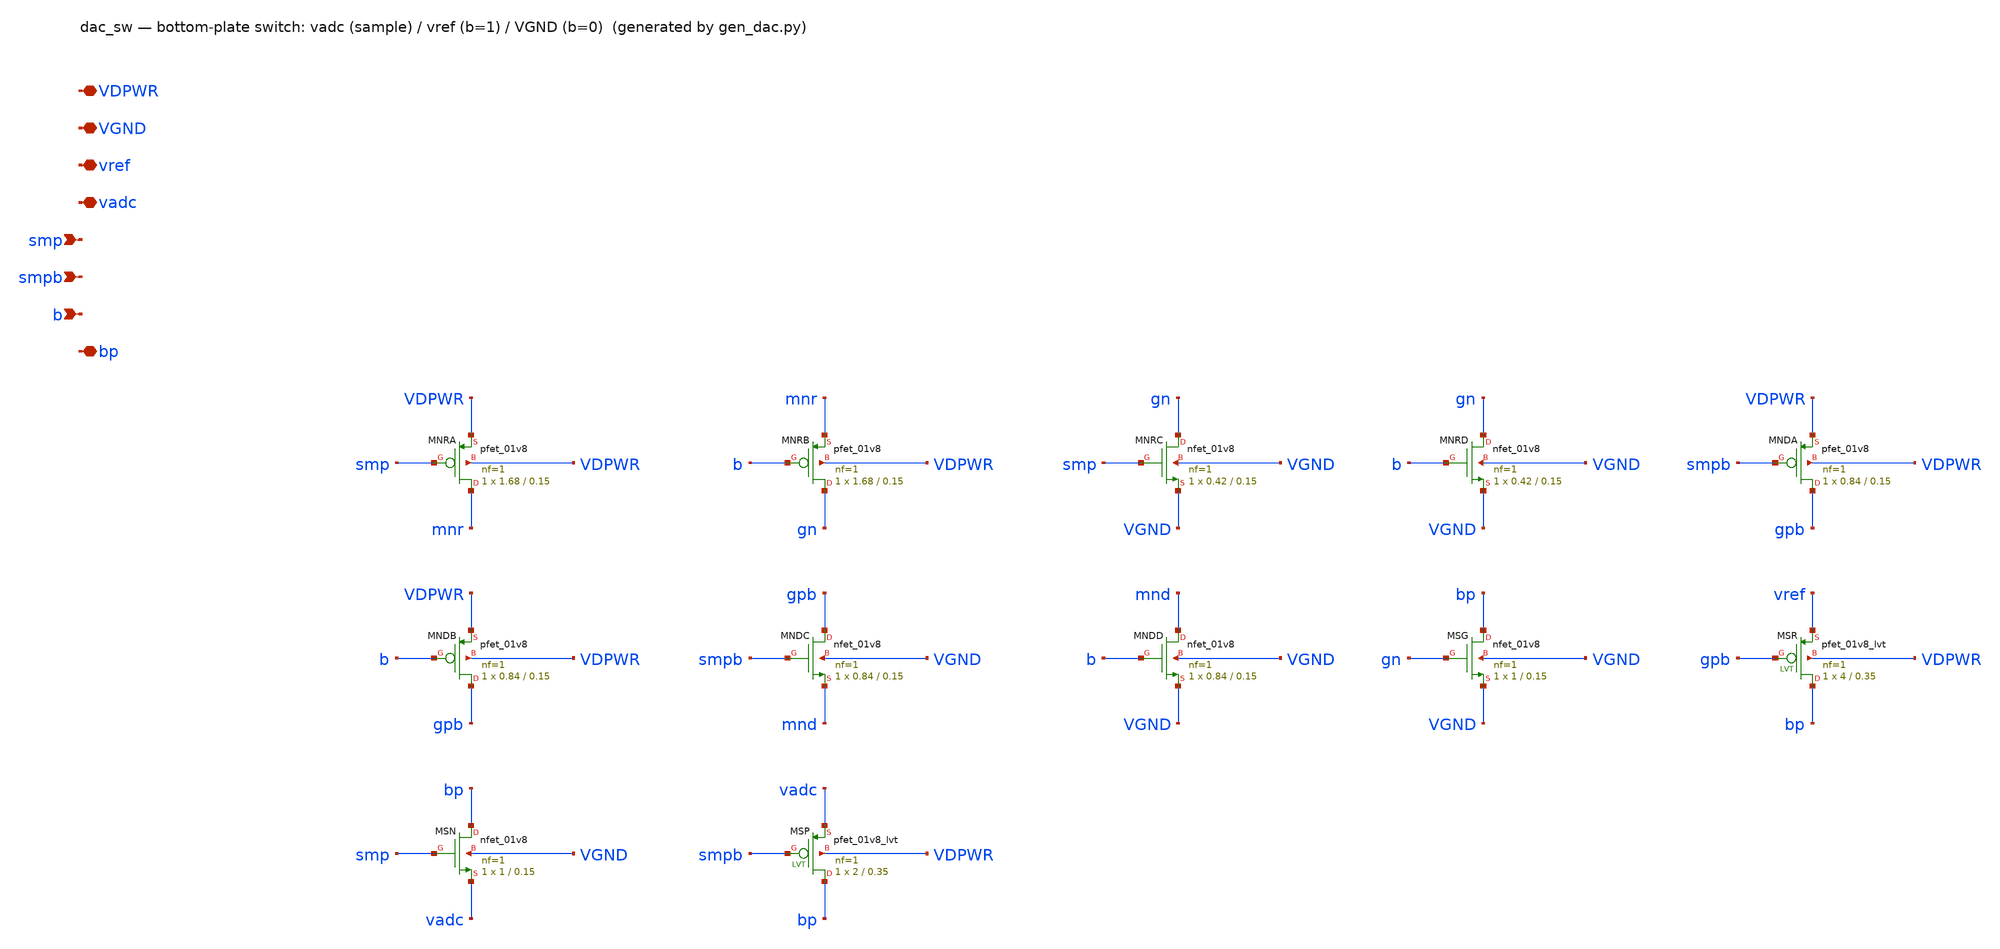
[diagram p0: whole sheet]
** sch_path: xschem/dac_sw.sch
**.subckt dac_sw VDPWR VGND vref vadc smp smpb b bp
*.iopin VDPWR
*.iopin VGND
*.iopin vref
*.iopin vadc
*.ipin smp
*.ipin smpb
*.ipin b
*.iopin bp
XMNRA mnr smp VDPWR VDPWR sky130_fd_pr__pfet_01v8 L=0.15 W=1.68 nf=1 ad='int((nf+1)/2) * W/nf * 0.29'
+ as='int((nf+2)/2) * W/nf * 0.29' pd='2*int((nf+1)/2) * (W/nf + 0.29)' ps='2*int((nf+2)/2) * (W/nf + 0.29)'
+ nrd='0.29 / W' nrs='0.29 / W' sa=0 sb=0 sd=0 mult=1 m=1
XMNRB gn b mnr VDPWR sky130_fd_pr__pfet_01v8 L=0.15 W=1.68 nf=1 ad='int((nf+1)/2) * W/nf * 0.29' as='int((nf+2)/2) * W/nf * 0.29'
+ pd='2*int((nf+1)/2) * (W/nf + 0.29)' ps='2*int((nf+2)/2) * (W/nf + 0.29)' nrd='0.29 / W' nrs='0.29 / W'
+ sa=0 sb=0 sd=0 mult=1 m=1
XMNRC gn smp VGND VGND sky130_fd_pr__nfet_01v8 L=0.15 W=0.42 nf=1 ad='int((1 + 1)/2) * 0.42 / 1 * 0.29'
+ as='int((1 + 2)/2) * 0.42 / 1 * 0.29' pd='2*int((1 + 1)/2) * (0.42 / 1 + 0.29)' ps='2*int((1 + 2)/2) * (0.42 / 1 + 0.29)'
+ nrd='0.29 / 0.42 ' nrs='0.29 / 0.42 ' sa=0 sb=0 sd=0 mult=1 m=1
XMNRD gn b VGND VGND sky130_fd_pr__nfet_01v8 L=0.15 W=0.42 nf=1 ad='int((1 + 1)/2) * 0.42 / 1 * 0.29'
+ as='int((1 + 2)/2) * 0.42 / 1 * 0.29' pd='2*int((1 + 1)/2) * (0.42 / 1 + 0.29)' ps='2*int((1 + 2)/2) * (0.42 / 1 + 0.29)'
+ nrd='0.29 / 0.42 ' nrs='0.29 / 0.42 ' sa=0 sb=0 sd=0 mult=1 m=1
XMNDA gpb smpb VDPWR VDPWR sky130_fd_pr__pfet_01v8 L=0.15 W=0.84 nf=1 ad='int((nf+1)/2) * W/nf * 0.29'
+ as='int((nf+2)/2) * W/nf * 0.29' pd='2*int((nf+1)/2) * (W/nf + 0.29)' ps='2*int((nf+2)/2) * (W/nf + 0.29)'
+ nrd='0.29 / W' nrs='0.29 / W' sa=0 sb=0 sd=0 mult=1 m=1
XMNDB gpb b VDPWR VDPWR sky130_fd_pr__pfet_01v8 L=0.15 W=0.84 nf=1 ad='int((nf+1)/2) * W/nf * 0.29' as='int((nf+2)/2) * W/nf * 0.29'
+ pd='2*int((nf+1)/2) * (W/nf + 0.29)' ps='2*int((nf+2)/2) * (W/nf + 0.29)' nrd='0.29 / W' nrs='0.29 / W'
+ sa=0 sb=0 sd=0 mult=1 m=1
XMNDC gpb smpb mnd VGND sky130_fd_pr__nfet_01v8 L=0.15 W=0.84 nf=1 ad='int((1 + 1)/2) * 0.84 / 1 * 0.29'
+ as='int((1 + 2)/2) * 0.84 / 1 * 0.29' pd='2*int((1 + 1)/2) * (0.84 / 1 + 0.29)' ps='2*int((1 + 2)/2) * (0.84 / 1 + 0.29)'
+ nrd='0.29 / 0.84 ' nrs='0.29 / 0.84 ' sa=0 sb=0 sd=0 mult=1 m=1
XMNDD mnd b VGND VGND sky130_fd_pr__nfet_01v8 L=0.15 W=0.84 nf=1 ad='int((1 + 1)/2) * 0.84 / 1 * 0.29'
+ as='int((1 + 2)/2) * 0.84 / 1 * 0.29' pd='2*int((1 + 1)/2) * (0.84 / 1 + 0.29)' ps='2*int((1 + 2)/2) * (0.84 / 1 + 0.29)'
+ nrd='0.29 / 0.84 ' nrs='0.29 / 0.84 ' sa=0 sb=0 sd=0 mult=1 m=1
XMSG bp gn VGND VGND sky130_fd_pr__nfet_01v8 L=0.15 W=1 nf=1 ad='int((1 + 1)/2) * 1 / 1 * 0.29' as='int((1 + 2)/2) * 1 / 1 * 0.29'
+ pd='2*int((1 + 1)/2) * (1 / 1 + 0.29)' ps='2*int((1 + 2)/2) * (1 / 1 + 0.29)' nrd='0.29 / 1 ' nrs='0.29 / 1 '
+ sa=0 sb=0 sd=0 mult=1 m=1
XMSR bp gpb vref VDPWR sky130_fd_pr__pfet_01v8_lvt L=0.35 W=4 nf=1 ad='int((1 + 1)/2) * 4 / 1 * 0.29'
+ as='int((1 + 2)/2) * 4 / 1 * 0.29' pd='2*int((1 + 1)/2) * (4 / 1 + 0.29)' ps='2*int((1 + 2)/2) * (4 / 1 + 0.29)'
+ nrd='0.29 / 4 ' nrs='0.29 / 4 ' sa=0 sb=0 sd=0 mult=1 m=1
XMSN bp smp vadc VGND sky130_fd_pr__nfet_01v8 L=0.15 W=1 nf=1 ad='int((1 + 1)/2) * 1 / 1 * 0.29' as='int((1 + 2)/2) * 1 / 1 * 0.29'
+ pd='2*int((1 + 1)/2) * (1 / 1 + 0.29)' ps='2*int((1 + 2)/2) * (1 / 1 + 0.29)' nrd='0.29 / 1 ' nrs='0.29 / 1 '
+ sa=0 sb=0 sd=0 mult=1 m=1
XMSP bp smpb vadc VDPWR sky130_fd_pr__pfet_01v8_lvt L=0.35 W=2 nf=1 ad='int((1 + 1)/2) * 2 / 1 * 0.29'
+ as='int((1 + 2)/2) * 2 / 1 * 0.29' pd='2*int((1 + 1)/2) * (2 / 1 + 0.29)' ps='2*int((1 + 2)/2) * (2 / 1 + 0.29)'
+ nrd='0.29 / 2 ' nrs='0.29 / 2 ' sa=0 sb=0 sd=0 mult=1 m=1
**.ends
.end
